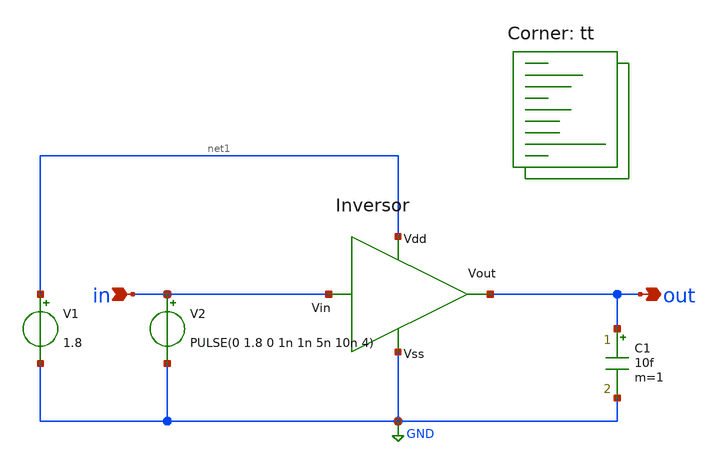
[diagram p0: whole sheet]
** sch_path: xschem/inversor_test.sch
**.subckt inversor_test in out
*.ipin in
*.opin out
x1 net1 out in GND inversor
V1 net1 GND 1.8
V2 in GND PULSE(0 1.8 0 1n 1n 5n 10n 4)
C1 out GND 10f m=1
**** begin user architecture code
.lib $::SKYWATER_MODELS/sky130.lib.spice tt


   .control
     run
     tran 0.01n 40n
     meas tran tphl TRIG v(in) VAL=0.9 RISE=1 TARG v(out) VAL=0.9 FALL=1
     meas tran tplh TRIG v(in) VAL=0.9 FALL=1 TARG v(out) VAL=0.9 RISE=1
     write inversor_test.raw
   .endc
   .save all


**** end user architecture code
**.ends

* expanding   symbol:  inversor.sym # of pins=4
** sym_path: xschem/inversor.sym
** sch_path: xschem/inversor.sch
.subckt inversor Vdd Vout Vin Vss
*.ipin Vdd
*.ipin Vss
*.opin Vout
*.ipin Vin
XM1 Vout Vin Vdd Vdd sky130_fd_pr__pfet_01v8 L=0.15 W=2.1 nf=1 ad='int((nf+1)/2) * W/nf * 0.29' as='int((nf+2)/2) * W/nf * 0.29'
+ pd='2*int((nf+1)/2) * (W/nf + 0.29)' ps='2*int((nf+2)/2) * (W/nf + 0.29)' nrd='0.29 / W' nrs='0.29 / W'
+ sa=0 sb=0 sd=0 mult=1 m=1
XM2 Vout Vin Vss Vss sky130_fd_pr__nfet_01v8 L=0.15 W=1.05 nf=1 ad='int((nf+1)/2) * W/nf * 0.29' as='int((nf+2)/2) * W/nf * 0.29'
+ pd='2*int((nf+1)/2) * (W/nf + 0.29)' ps='2*int((nf+2)/2) * (W/nf + 0.29)' nrd='0.29 / W' nrs='0.29 / W'
+ sa=0 sb=0 sd=0 mult=1 m=1
.ends

.GLOBAL GND
.end
